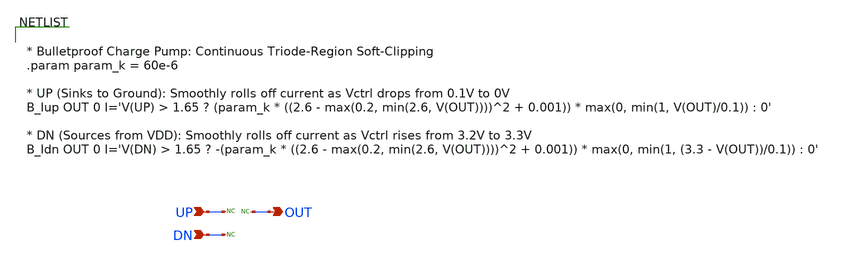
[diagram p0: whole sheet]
** sch_path: designs/libs/model_pll/CP_model.sch
**.subckt CP_model UP DN OUT
*.ipin UP
*.ipin DN
*.opin OUT
* noconn UP
* noconn DN
* noconn OUT
**** begin user architecture code


* Bulletproof Charge Pump: Continuous Triode-Region Soft-Clipping
.param param_k = 60e-6

* UP (Sinks to Ground): Smoothly rolls off current as Vctrl drops from 0.1V to 0V
B_Iup OUT 0 I='V(UP) > 1.65 ? (param_k * ((2.6 - max(0.2, min(2.6, V(OUT))))^2 + 0.001)) * max(0, min(1, V(OUT)/0.1)) : 0'

* DN (Sources from VDD): Smoothly rolls off current as Vctrl rises from 3.2V to 3.3V
B_Idn OUT 0 I='V(DN) > 1.65 ? -(param_k * ((2.6 - max(0.2, min(2.6, V(OUT))))^2 + 0.001)) * max(0, min(1, (3.3 - V(OUT))/0.1)) : 0'


**** end user architecture code
**.ends
.end
